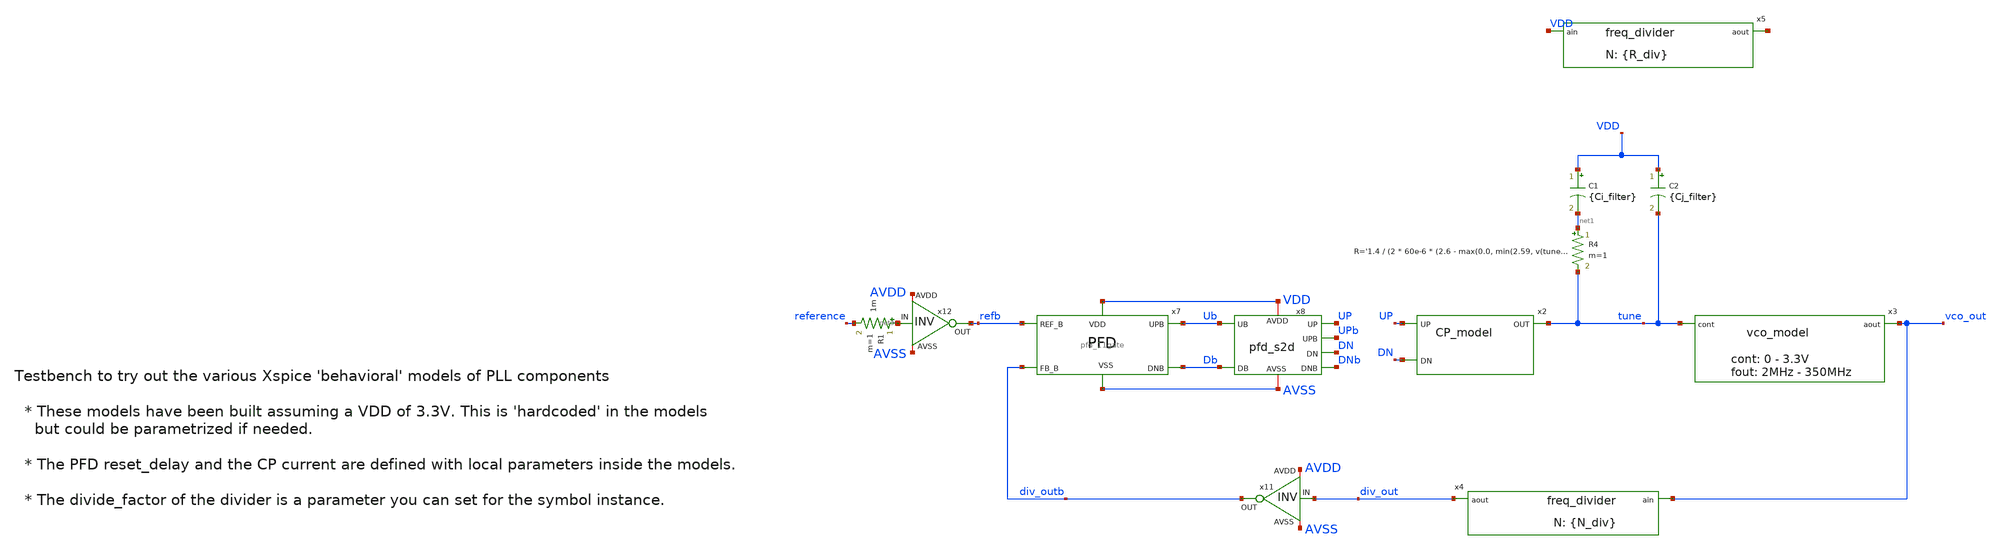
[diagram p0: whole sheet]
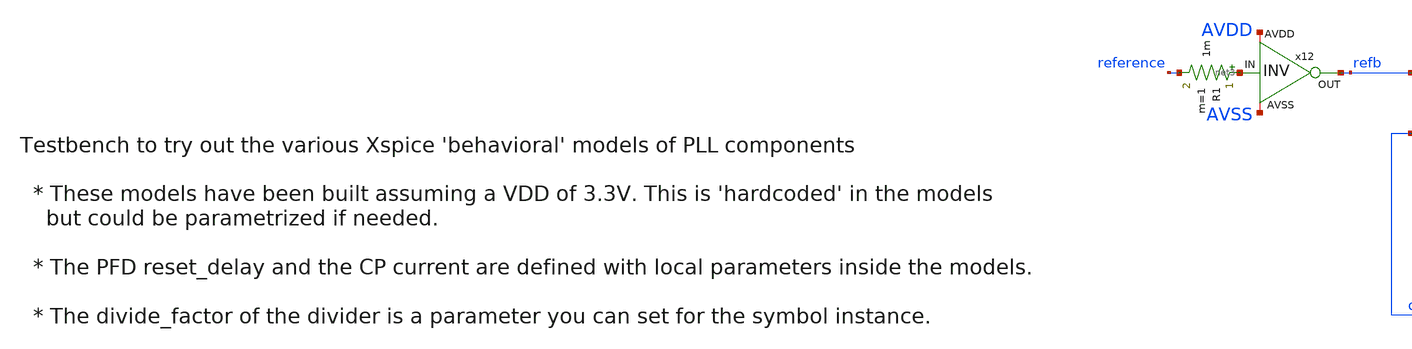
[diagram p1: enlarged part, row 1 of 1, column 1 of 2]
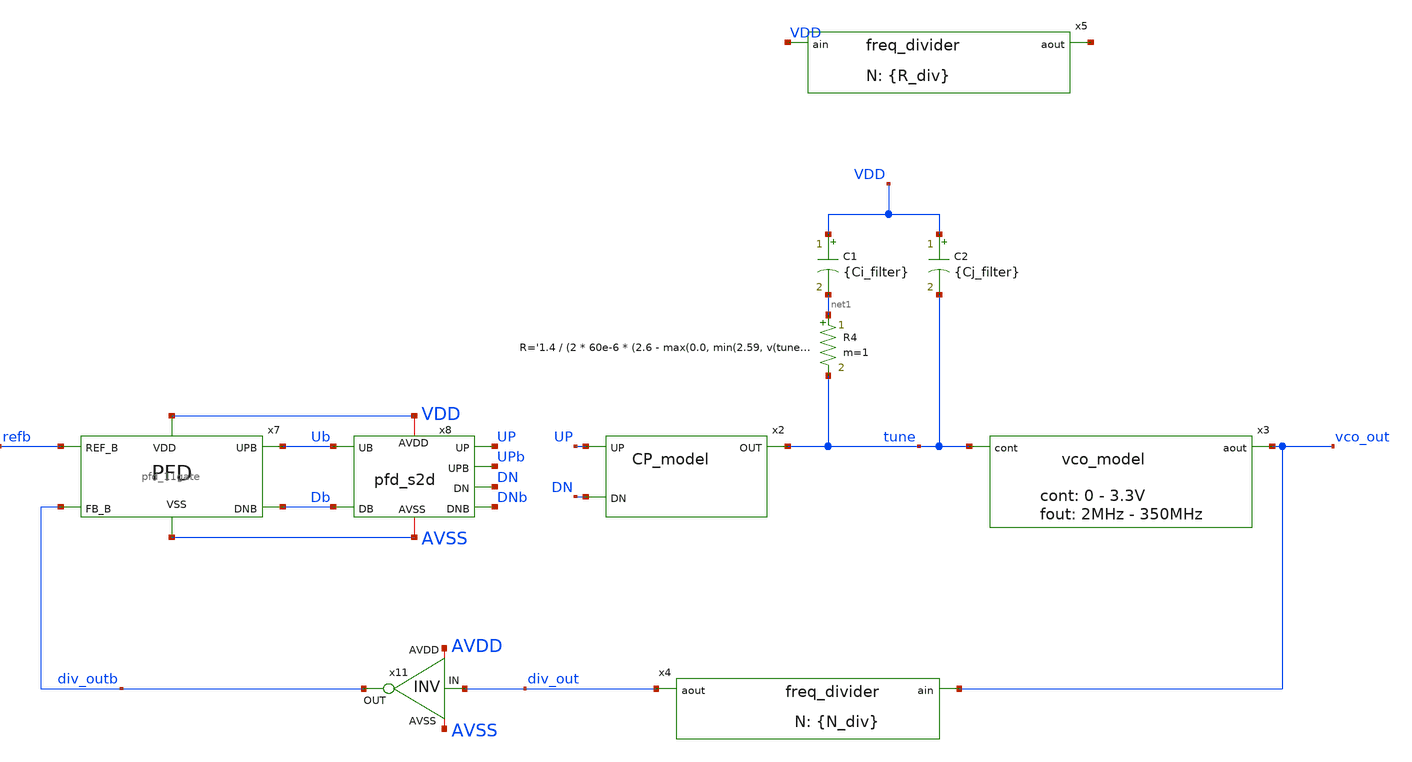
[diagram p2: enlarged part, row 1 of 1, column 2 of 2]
** sch_path: designs/libs/tb_pll/tb_PLL_PFD_model.sch
**.subckt tb_PLL_PFD_model
C1 VDD net1 {Ci_filter} m=1
R4 net1 tune R='1.4 / (2 * 60e-6 * (2.6 - max(0.0, min(2.59, v(tune)))))' m=1
C2 VDD tune {Cj_filter} m=1
x2 tune UP DN CP_model
x3 vco_out tune vco_model
x4 div_out vco_out freq_divider divide_factor={N_div}
x5 net2 VDD freq_divider divide_factor={R_div}
x7 refb Ub Db div_outb VDD AVSS pfd_11gate
x8 UPb Ub UP VDD AVSS DNb Db DN pfd_s2d
x11 AVDD div_out div_outb AVSS inv
x12 AVDD net3 refb AVSS inv
R1 net3 reference 1m m=1
**** begin user architecture code

.include /foss/pdks/ciel/gf180mcu/versions/7b70722e33c03fcb5dabcf4d479fb0822d9251c9/gf180mcuD/libs.ref/gf180mcu_fd_sc_mcu7t5v0/spice/gf180mcu_fd_sc_mcu7t5v0.spice
.include $::180MCU_MODELS/design.ngspice
.lib $::180MCU_MODELS/sm141064.ngspice typical



.options method=gear
VDD VDD 0 3.3
VAVDD AVDD 0 3.3
Vss AVSS 0 0

.options reltol=1e-5 cshunt=1e-15 itl4=50 gmin=1e-12
.options method=gear

* control is for tests when opening the loop
* see the Vcontrol voltage source
.ic v(tune)=2
* reference frequency
.param f_ref = 10MEG
* divider
.param R_div=2
.param N_div=35
* loop filter parameters
.param Ci_filter = 10p
.param Cj_filter = 1p
.param td_ref='1/f_ref' tp_ref='td_ref/2'
Vref reference gnd pulse(0 3.3 0 100p 100p tp_ref td_ref)

.control
set wr_singlescale
set wr_vecnames

*save all
save v(vco_out) v(reference) v(up) v(dn) v(tune)

TRAN 100p 100u
linearize v(vco_out) v(reference) v(up) v(dn) v(tune)
*fft v(vco_out)

write tb_PLL_PFD_model2.raw
wrdata /foss/designs/synchronos-chipathon-2026/designs/libs/scripts/sim_data/tb_PLL_PFD_model2.txt
+ tran.all
.endc


**** end user architecture code
**.ends
.end
